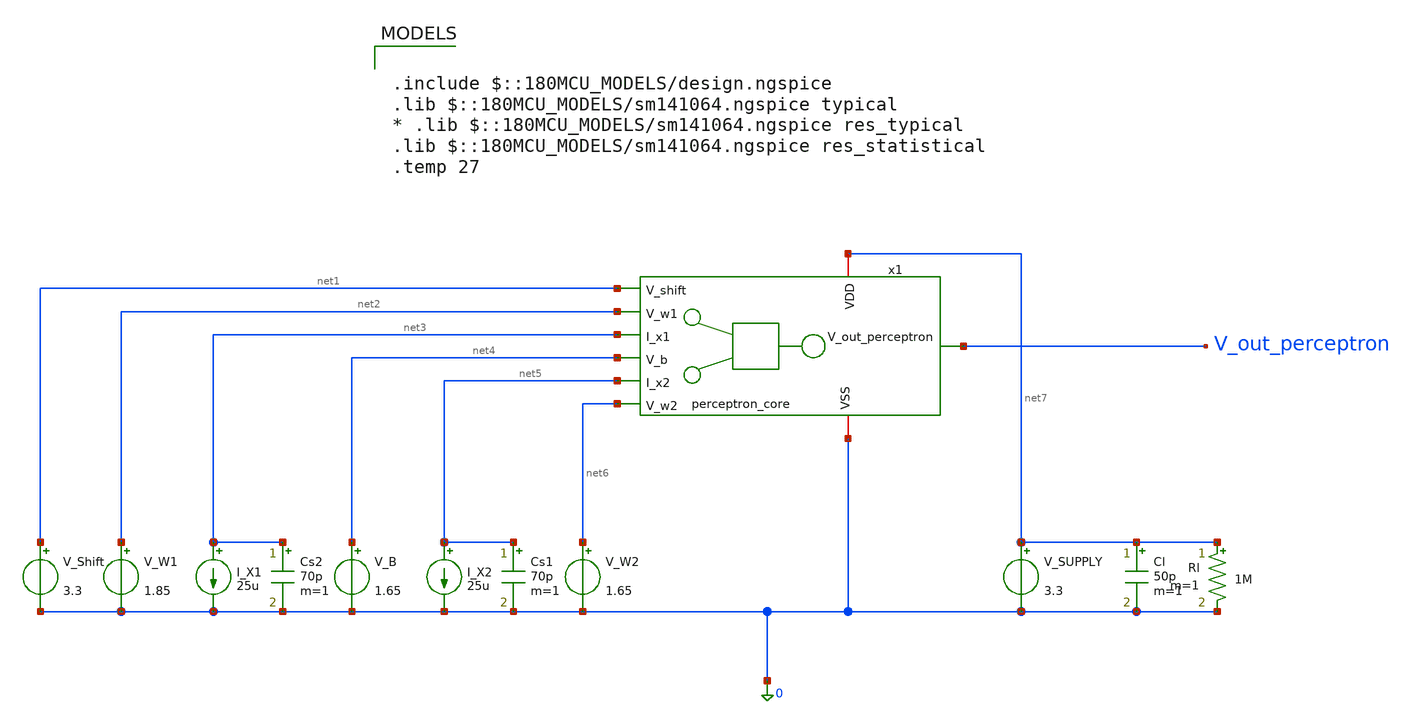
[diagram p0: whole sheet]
** sch_path: lvs/schematics/tb_realistic_perceptron_core.sch
**.subckt tb_realistic_perceptron_core
V_SUPPLY net7 0 3.3
V_Shift net1 0 3.3
Cs1 net5 0 70p m=1
Cs2 net3 0 70p m=1
Cl net7 0 50p m=1
Rl net7 0 1M m=1
I_X1 net3 0 25u
I_X2 net5 0 25u
V_W1 net2 0 1.85
V_W2 net6 0 1.65
V_B net4 0 1.65
x1 net7 net1 net2 net3 V_out_perceptron net4 net5 net6 0 perceptron_core
**** begin user architecture code


.control
  * --- start from neutral ---
  alter V_W1 = 1.65
  alter V_W2 = 1.65
  alter V_B  = 1.65
  alter I_X1 = 0
  alter I_X2 = 0

  * === Transient Analysis ===
  * Applying a 50uA pulse to I_X1 to observe step response and settling
  alter @I_X1[pulse] = [ 0 50u 1u 10n 10n 10u 20u ]
  alter I_X2 = 0
  alter V_W1 = 1.85
  alter V_W2 = 1.65
  alter V_B  = 1.65
  tran 10n 30u
  wrdata /foss/designs/analog-perceptron-gf180mcu/plots/real_tran_perceptron.txt v(V_out_perceptron)
  alter @I_X1[pulse] = [ 0 0 0 0 0 0 0 ] $ Clear pulse after tran

  * === AC Analysis (Stability & Bandwidth) ===
  * Injecting AC signal into I_X1
  alter I_X1 = 25u
  alter @I_X1[acmag] = 1
  alter V_W1 = 1.85
  ac dec 20 1 1G
  * wrdata exports real and imaginary parts for AC.
  wrdata /foss/designs/analog-perceptron-gf180mcu/plots/real_ac_perceptron.txt v(V_out_perceptron)
  alter @I_X1[acmag] = 0 $ Clear AC magnitude
  alter I_X1 = 0

  * === Return to global environment before loops ===
  reset
  setplot const

  * === Graph 1: Weight sweep (inhibitory / neutral / excitatory) ===
  alter I_X2 = 0
  alter V_W2 = 1.65
  alter V_B  = 1.65
  let n = 0
  dowhile n <= 2
    let vw1 = 1.45 + n * 0.2
    alter V_W1 = vw1
    dc I_X1 0 50u 1u
    wrdata /foss/designs/analog-perceptron-gf180mcu/plots/real_perceptron_graph1_weights.txt
+ v(V_out_perceptron)
    set appendwrite
    let n = n + 1
  end
  unset appendwrite
  alter V_W1 = 1.65

  * === Graph 2: Sensor 1 sweep, Sensor 2 interference ===
  alter V_W1 = 1.85
  alter V_W2 = 1.85
  alter V_B  = 1.65
  let n = 0
  dowhile n <= 2
    let ix2 = n * 25u
    alter I_X2 = ix2
    dc I_X1 0 50u 1u
    wrdata /foss/designs/analog-perceptron-gf180mcu/plots/real_perceptron_graph2_sensors.txt
+ v(V_out_perceptron)
    set appendwrite
    let n = n + 1
  end
  unset appendwrite
  alter V_W1 = 1.65
  alter V_W2 = 1.65
  alter I_X2 = 0

  * === Graph 3: Bias shifting ===
  alter I_X2 = 0
  alter V_W1 = 1.85
  let n = 0
  dowhile n <= 2
    let vb = 1.45 + n * 0.2
    alter V_B = vb
    dc I_X1 0 50u 1u
    wrdata /foss/designs/analog-perceptron-gf180mcu/plots/real_perceptron_graph3_bias.txt
+ v(V_out_perceptron)
    set appendwrite
    let n = n + 1
  end
  unset appendwrite
  alter V_W1 = 1.65
  alter V_B  = 1.65

  * === Graph 4: V_Shift sweep (reference-rail sensitivity / corner check) ===
  alter I_X2 = 0
  alter V_W1 = 1.85
  alter V_B  = 1.65
  let n = 0
  dowhile n <= 5
    let vshift = 3.25 + n * 0.02
    alter V_Shift = vshift
    dc I_X1 0 50u 1u
    wrdata /foss/designs/analog-perceptron-gf180mcu/plots/real_perceptron_graph4_vshift.txt
+ v(V_out_perceptron)
    set appendwrite
    let n = n + 1
  end
  unset appendwrite
  alter V_Shift = 3.3
  alter V_W1 = 1.65

  * === 3D Dataset A: I_X1 x I_X2 -> V_out ===
  alter V_W1 = 1.85
  alter V_W2 = 1.85
  alter V_B  = 1.65
  let n = 0
  dowhile n <= 25
    let ix2b = n * 2u
    alter I_X2 = ix2b
    dc I_X1 0 50u 1u
    wrdata /foss/designs/analog-perceptron-gf180mcu/plots/real_3d_sensors.txt v(V_out_perceptron)
    set appendwrite
    let n = n + 1
  end
  unset appendwrite
  alter V_W1 = 1.65
  alter V_W2 = 1.65
  alter I_X2 = 0

  * === 3D Dataset B: V_W1 x V_W2 -> V_out ===
  alter I_X1 = 50u
  alter I_X2 = 50u
  alter V_B  = 1.65
  let n = 0
  dowhile n <= 20
    let vw2 = 1.45 + n * 0.02
    alter V_W2 = vw2
    dc V_W1 1.45 1.85 0.01
    wrdata /foss/designs/analog-perceptron-gf180mcu/plots/real_3d_weights.txt v(V_out_perceptron)
    set appendwrite
    let n = n + 1
  end
  unset appendwrite
  alter V_W1 = 1.65
  alter V_W2 = 1.65
  alter V_B  = 1.65
  alter I_X1 = 0
  alter I_X2 = 0

  * === OP-SWEEP DIAGNOSTIC: all devices ===
  alter V_W1 = 1.85
  alter V_W2 = 1.65
  alter V_B  = 1.65
  alter I_X2 = 0
  save all @m.x1.x1.xm1.m0[vgs] @m.x1.x1.xm1.m0[vth] @m.x1.x1.xm1.m0[id] @m.x1.x2.xm1.m0[vgs]
+ @m.x1.x2.xm1.m0[vth] @m.x1.x2.xm1.m0[id] @m.x1.x_g1.xm7.m0[vgs] @m.x1.x_g1.xm7.m0[vth] @m.x1.x_g1.xm7.m0[id]
+ @m.x1.x_g2.xm7.m0[vgs] @m.x1.x_g2.xm7.m0[vth] @m.x1.x_g2.xm7.m0[id] @m.x1.x_g3.xm7.m0[vgs] @m.x1.x_g3.xm7.m0[vth]
+ @m.x1.x_g3.xm7.m0[id] @m.x1.x_tanh.xm1.m0[vgs] @m.x1.x_tanh.xm1.m0[vth] @m.x1.x_tanh.xm1.m0[id] @m.x1.x_tanh.xm2.m0[vgs]
+ @m.x1.x_tanh.xm2.m0[vth] @m.x1.x_tanh.xm2.m0[id]
  dc I_X1 0 50u 1u
  wrdata /foss/designs/analog-perceptron-gf180mcu/plots/real_opsweep_perceptron_chain.txt
+ v(V_out_perceptron) @m.x1.x1.xm1.m0[vgs] @m.x1.x1.xm1.m0[vth] @m.x1.x1.xm1.m0[id] @m.x1.x2.xm1.m0[vgs]
+ @m.x1.x2.xm1.m0[vth] @m.x1.x2.xm1.m0[id] @m.x1.x_g1.xm7.m0[vgs] @m.x1.x_g1.xm7.m0[vth] @m.x1.x_g1.xm7.m0[id]
+ @m.x1.x_g2.xm7.m0[vgs] @m.x1.x_g2.xm7.m0[vth] @m.x1.x_g2.xm7.m0[id] @m.x1.x_g3.xm7.m0[vgs] @m.x1.x_g3.xm7.m0[vth]
+ @m.x1.x_g3.xm7.m0[id] @m.x1.x_tanh.xm1.m0[vgs] @m.x1.x_tanh.xm1.m0[vth] @m.x1.x_tanh.xm1.m0[id] @m.x1.x_tanh.xm2.m0[vgs]
+ @m.x1.x_tanh.xm2.m0[vth] @m.x1.x_tanh.xm2.m0[id]
  alter V_W1 = 1.65
  alter V_W2 = 1.65
  alter V_B  = 1.65
  alter I_X1 = 0
  alter I_X2 = 0

  * === OP-SWEEP DIAGNOSTIC #2: all devices, I_X2 swept ===
  alter V_W1 = 1.85
  alter V_W2 = 1.65
  alter V_B  = 1.65
  alter I_X1 = 25u
  save all @m.x1.x1.xm1.m0[vgs] @m.x1.x1.xm1.m0[vth] @m.x1.x1.xm1.m0[id] @m.x1.x2.xm1.m0[vgs]
+ @m.x1.x2.xm1.m0[vth] @m.x1.x2.xm1.m0[id] @m.x1.x_g1.xm7.m0[vgs] @m.x1.x_g1.xm7.m0[vth] @m.x1.x_g1.xm7.m0[id]
+ @m.x1.x_g2.xm7.m0[vgs] @m.x1.x_g2.xm7.m0[vth] @m.x1.x_g2.xm7.m0[id] @m.x1.x_g3.xm7.m0[vgs] @m.x1.x_g3.xm7.m0[vth]
+ @m.x1.x_g3.xm7.m0[id] @m.x1.x_tanh.xm1.m0[vgs] @m.x1.x_tanh.xm1.m0[vth] @m.x1.x_tanh.xm1.m0[id] @m.x1.x_tanh.xm2.m0[vgs]
+ @m.x1.x_tanh.xm2.m0[vth] @m.x1.x_tanh.xm2.m0[id]
  dc I_X2 0 50u 1u
  wrdata /foss/designs/analog-perceptron-gf180mcu/plots/real_opsweep_perceptron_chain_ix2.txt
+ v(V_out_perceptron) @m.x1.x1.xm1.m0[vgs] @m.x1.x1.xm1.m0[vth] @m.x1.x1.xm1.m0[id] @m.x1.x2.xm1.m0[vgs]
+ @m.x1.x2.xm1.m0[vth] @m.x1.x2.xm1.m0[id] @m.x1.x_g1.xm7.m0[vgs] @m.x1.x_g1.xm7.m0[vth] @m.x1.x_g1.xm7.m0[id]
+ @m.x1.x_g2.xm7.m0[vgs] @m.x1.x_g2.xm7.m0[vth] @m.x1.x_g2.xm7.m0[id] @m.x1.x_g3.xm7.m0[vgs] @m.x1.x_g3.xm7.m0[vth]
+ @m.x1.x_g3.xm7.m0[id] @m.x1.x_tanh.xm1.m0[vgs] @m.x1.x_tanh.xm1.m0[vth] @m.x1.x_tanh.xm1.m0[id] @m.x1.x_tanh.xm2.m0[vgs]
+ @m.x1.x_tanh.xm2.m0[vth] @m.x1.x_tanh.xm2.m0[id]
.endc



.include $::180MCU_MODELS/design.ngspice
.lib $::180MCU_MODELS/sm141064.ngspice typical
* .lib $::180MCU_MODELS/sm141064.ngspice res_typical
.lib $::180MCU_MODELS/sm141064.ngspice res_statistical
.temp 27

**** end user architecture code
**.ends
.end
